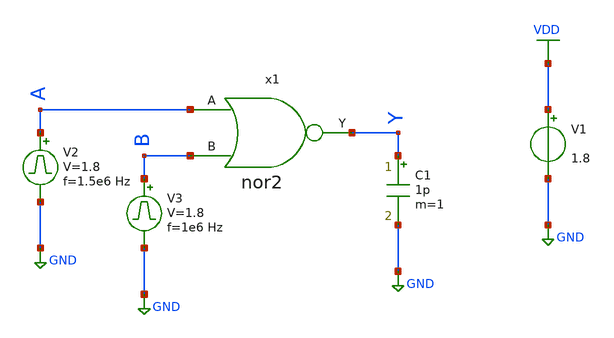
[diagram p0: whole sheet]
** sch_path: library/xschem/nor2_tb.sch
**.subckt nor2_tb
V1 VDD GND 1.8
V2 A GND pulse 0 1.8 '0.495/ 1.5e6 ' '0.01/1.5e6 ' '0.01/1.5e6 ' '0.49/1.5e6 ' '1/1.5e6 '
C1 Y GND 1p m=1
V3 B GND pulse 0 1.8 '0.495/ 1e6 ' '0.01/1e6 ' '0.01/1e6 ' '0.49/1e6 ' '1/1e6 '
x1 A B Y nor2
**** begin user architecture code


.control
save all
tran 1n 2u
plot V(A) V(B) V(Y)
.endc


** opencircuitdesign pdks install
.lib $::SKYWATER_MODELS/sky130.lib.spice tt


**** end user architecture code
**.ends

* expanding   symbol:  nor2.sym # of pins=3
** sym_path: library/xschem/nor2.sym
** sch_path: library/xschem/nor2.sch
.subckt nor2 A B Y
*.opin Y
*.ipin A
*.ipin B
XM1 Y B GND GND sky130_fd_pr__nfet_01v8 L=0.15 W=1 nf=1 ad='int((nf+1)/2) * W/nf * 0.29' as='int((nf+2)/2) * W/nf * 0.29'
+ pd='2*int((nf+1)/2) * (W/nf + 0.29)' ps='2*int((nf+2)/2) * (W/nf + 0.29)' nrd='0.29 / W' nrs='0.29 / W'
+ sa=0 sb=0 sd=0 mult=1 m=1
XM2 Y B net1 VDD sky130_fd_pr__pfet_01v8 L=0.15 W=1 nf=1 ad='int((nf+1)/2) * W/nf * 0.29' as='int((nf+2)/2) * W/nf * 0.29'
+ pd='2*int((nf+1)/2) * (W/nf + 0.29)' ps='2*int((nf+2)/2) * (W/nf + 0.29)' nrd='0.29 / W' nrs='0.29 / W'
+ sa=0 sb=0 sd=0 mult=1 m=1
XM3 net1 A VDD VDD sky130_fd_pr__pfet_01v8 L=0.15 W=1 nf=1 ad='int((nf+1)/2) * W/nf * 0.29' as='int((nf+2)/2) * W/nf * 0.29'
+ pd='2*int((nf+1)/2) * (W/nf + 0.29)' ps='2*int((nf+2)/2) * (W/nf + 0.29)' nrd='0.29 / W' nrs='0.29 / W'
+ sa=0 sb=0 sd=0 mult=1 m=1
XM4 Y A GND GND sky130_fd_pr__nfet_01v8 L=0.15 W=1 nf=1 ad='int((nf+1)/2) * W/nf * 0.29' as='int((nf+2)/2) * W/nf * 0.29'
+ pd='2*int((nf+1)/2) * (W/nf + 0.29)' ps='2*int((nf+2)/2) * (W/nf + 0.29)' nrd='0.29 / W' nrs='0.29 / W'
+ sa=0 sb=0 sd=0 mult=1 m=1
.ends

.GLOBAL VDD
.GLOBAL GND
.end
